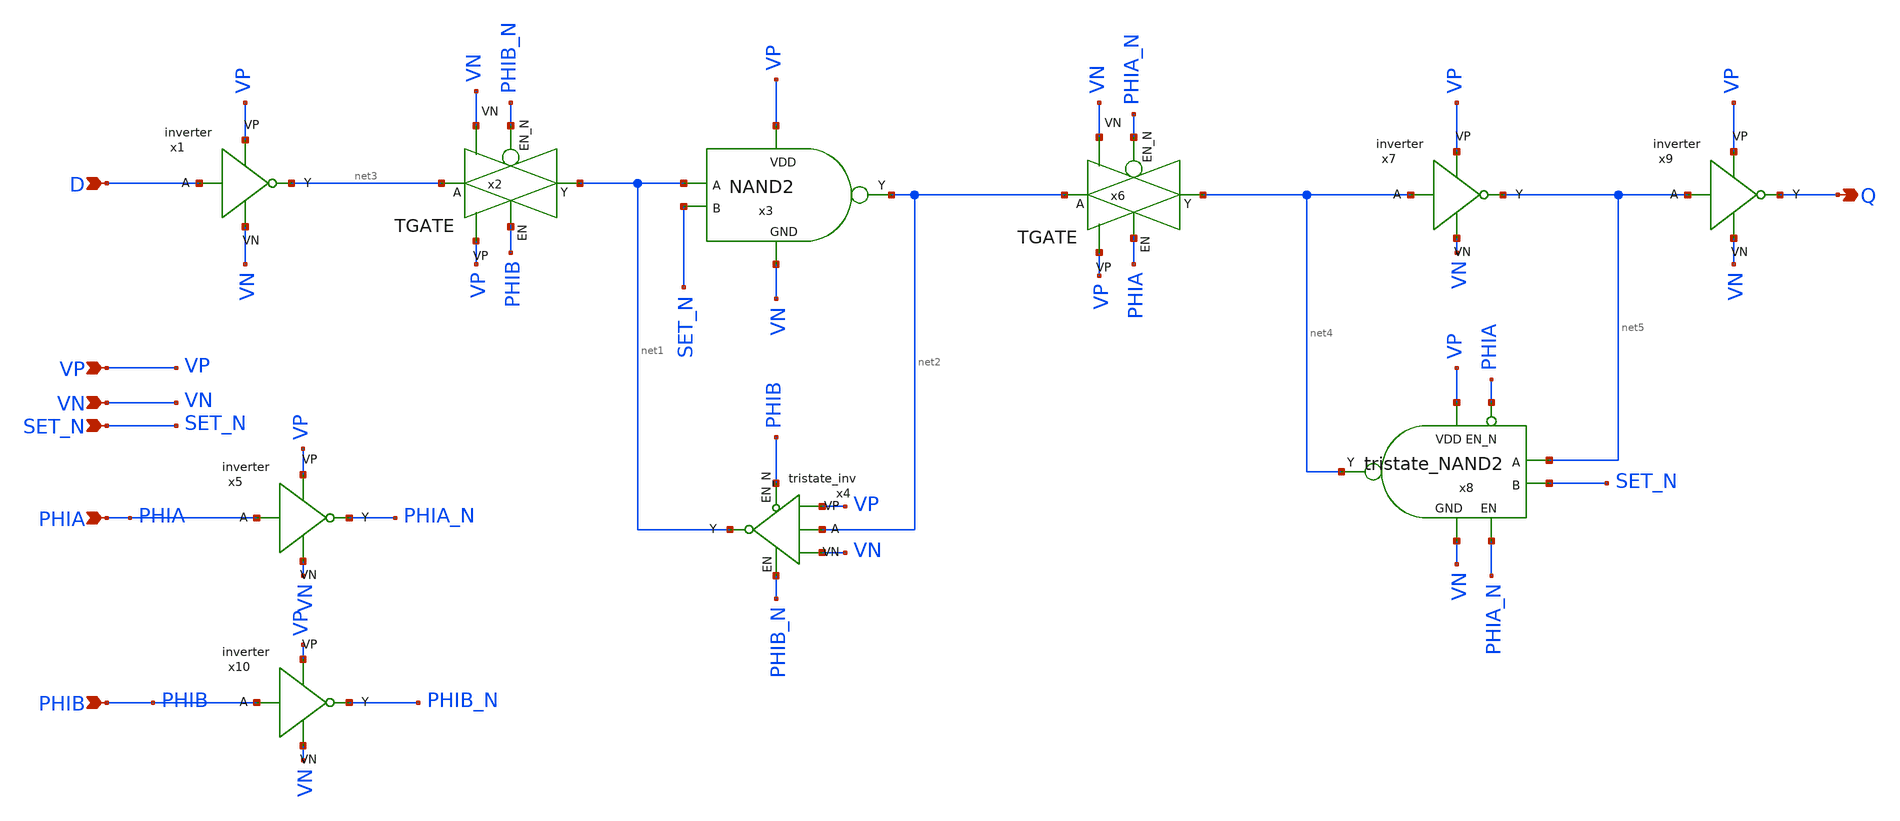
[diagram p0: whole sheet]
** sch_path: ADC/16bit_C2C/MagicAndSpice/EE431_FinalProj/DFFS.sch
**.subckt DFFS D VN SET_N VP Q PHIB PHIA
*.ipin D
*.ipin VN
*.ipin SET_N
*.ipin VP
*.opin Q
*.ipin PHIB
*.ipin PHIA
x1 D net3 VP VN inverter
x2 net3 net1 PHIB PHIB_N TGATE
x3 VP net2 net1 SET_N VN NAND2
x4 net2 net1 PHIB_N PHIB VP VN tristate_inv
x6 net2 net4 PHIA PHIA_N TGATE
x7 net4 net5 VP VN inverter
x8 net5 SET_N net4 PHIA_N PHIA VP VN tristate_NAND2
x9 net5 Q VP VN inverter
x5 PHIA PHIA_N VP VN inverter
x10 PHIB PHIB_N VP VN inverter
**.ends
.end
